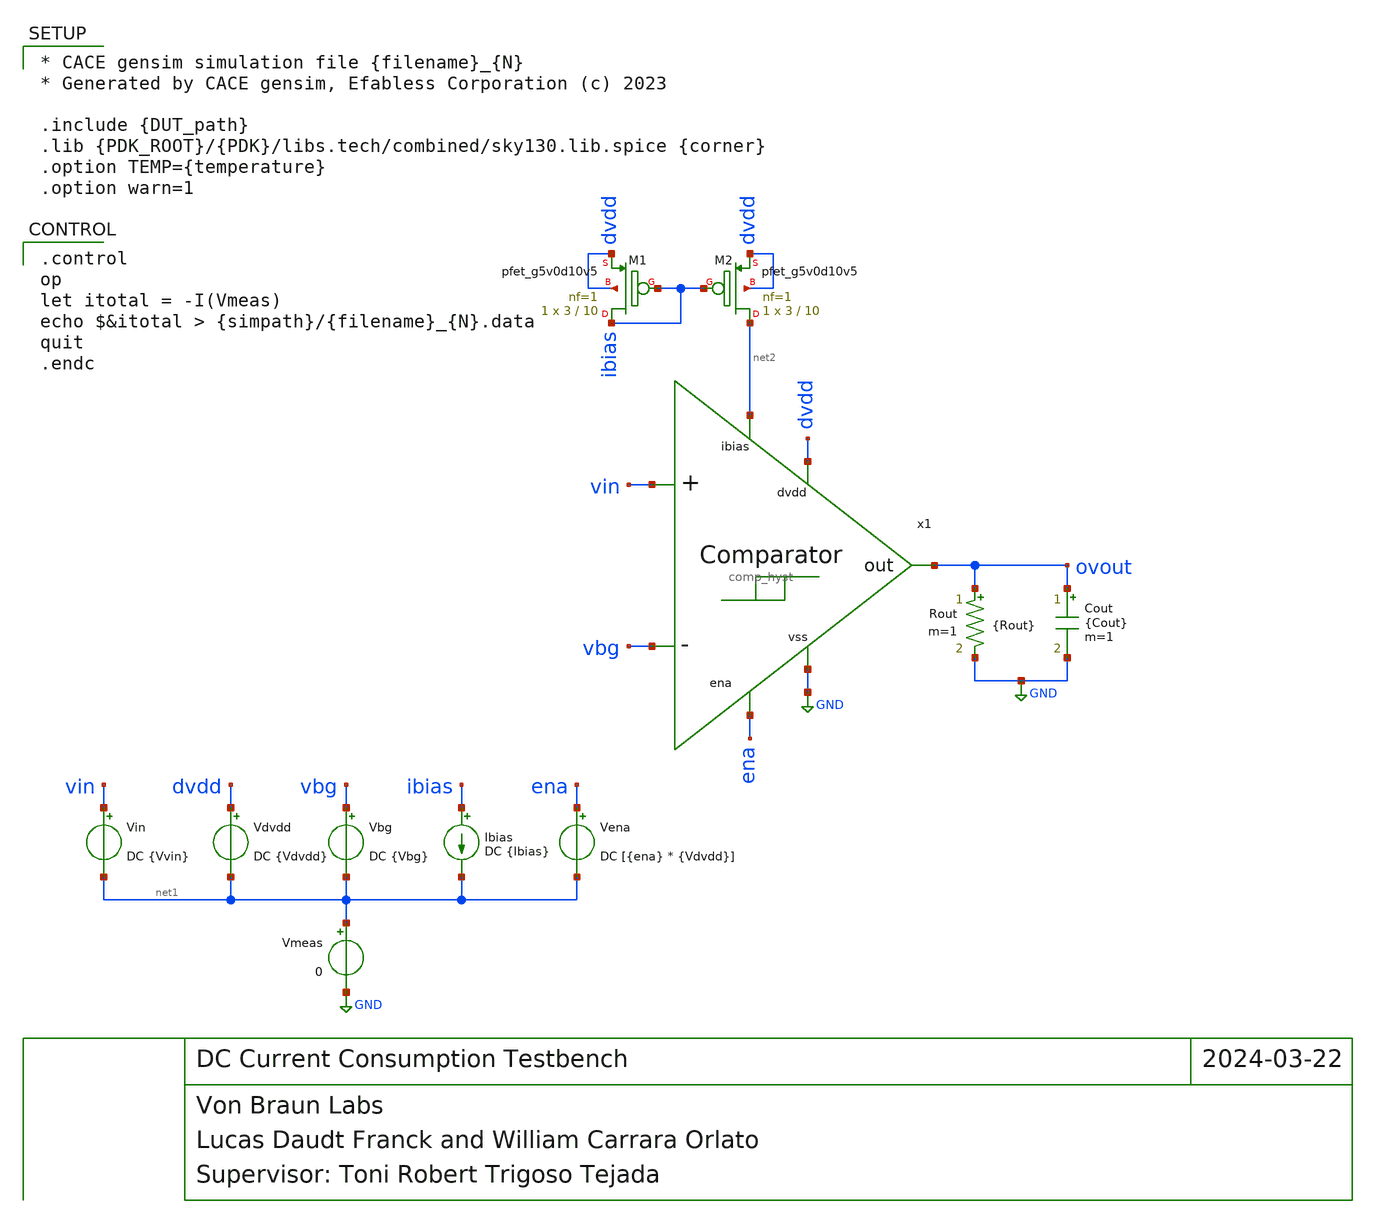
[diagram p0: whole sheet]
** sch_path: blocks/comp_hyst/cace/tb_dccurrent.sch
**.subckt tb_dccurrent
Cout ovout GND {Cout} m=1
Rout ovout GND {Rout} m=1
Vin vin net1 DC {Vvin}
Vdvdd dvdd net1 DC {Vdvdd}
Vena ena net1 DC [{ena} * {Vdvdd}]
Vbg vbg net1 DC {Vbg}
Ibias ibias net1 DC {Ibias}
Vmeas net1 GND 0
x1 dvdd ovout vbg vin ena net2 GND comp_hyst
XM1 ibias ibias dvdd dvdd sky130_fd_pr__pfet_g5v0d10v5 L=10 W=3 nf=1 ad='int((nf+1)/2) * W/nf * 0.29'
+ as='int((nf+2)/2) * W/nf * 0.29' pd='2*int((nf+1)/2) * (W/nf + 0.29)' ps='2*int((nf+2)/2) * (W/nf + 0.29)'
+ nrd='0.29 / W' nrs='0.29 / W' sa=0 sb=0 sd=0 mult=1 m=1
XM2 net2 ibias dvdd dvdd sky130_fd_pr__pfet_g5v0d10v5 L=10 W=3 nf=1 ad='int((nf+1)/2) * W/nf * 0.29'
+ as='int((nf+2)/2) * W/nf * 0.29' pd='2*int((nf+1)/2) * (W/nf + 0.29)' ps='2*int((nf+2)/2) * (W/nf + 0.29)'
+ nrd='0.29 / W' nrs='0.29 / W' sa=0 sb=0 sd=0 mult=1 m=1
**** begin user architecture code

* CACE gensim simulation file {filename}_{N}
* Generated by CACE gensim, Efabless Corporation (c) 2023

.include {DUT_path}
.lib {PDK_ROOT}/{PDK}/libs.tech/combined/sky130.lib.spice {corner}
.option TEMP={temperature}
.option warn=1



.control
op
let itotal = -I(Vmeas)
echo $&itotal > {simpath}/{filename}_{N}.data
quit
.endc


**** end user architecture code
**.ends
.GLOBAL GND
.end
